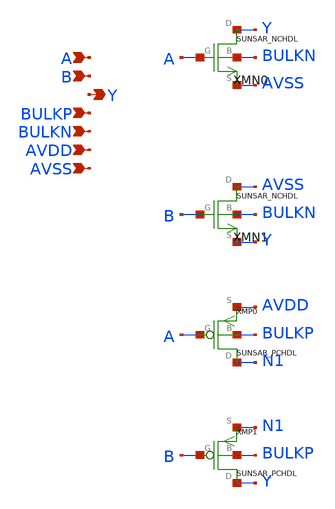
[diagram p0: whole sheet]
** sch_path: ip/sun_sar9b_sky130nm/design/SUN_SAR9B_SKY130NM/SUNSAR_NRX1_CV.sch
**.subckt SUNSAR_NRX1_CV A B Y BULKP BULKN AVDD AVSS
*.ipin A
*.ipin B
*.opin Y
*.ipin BULKP
*.ipin BULKN
*.ipin AVDD
*.ipin AVSS
XMN0 Y A AVSS BULKN SUNSAR_NCHDL
XMN1 AVSS B Y BULKN SUNSAR_NCHDL
XMP0 N1 A AVDD BULKP SUNSAR_PCHDL
XMP1 Y B N1 BULKP SUNSAR_PCHDL
**.ends
.end
